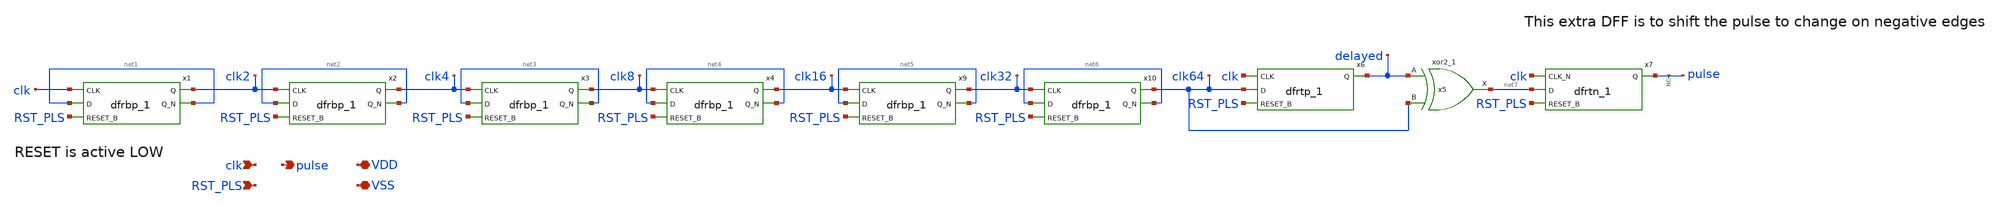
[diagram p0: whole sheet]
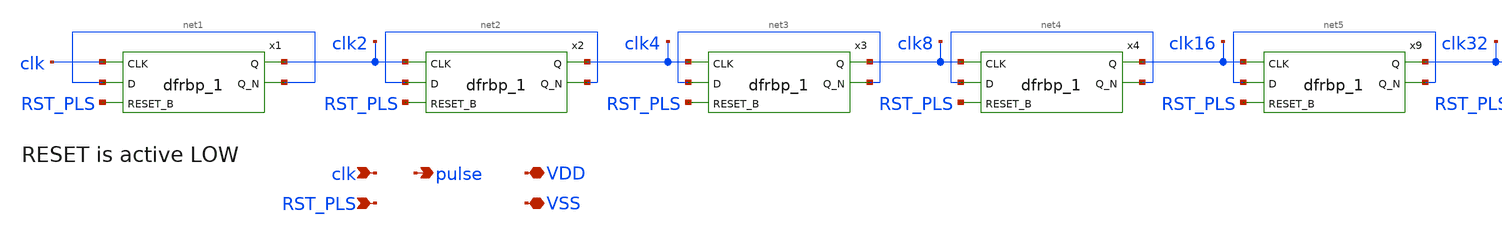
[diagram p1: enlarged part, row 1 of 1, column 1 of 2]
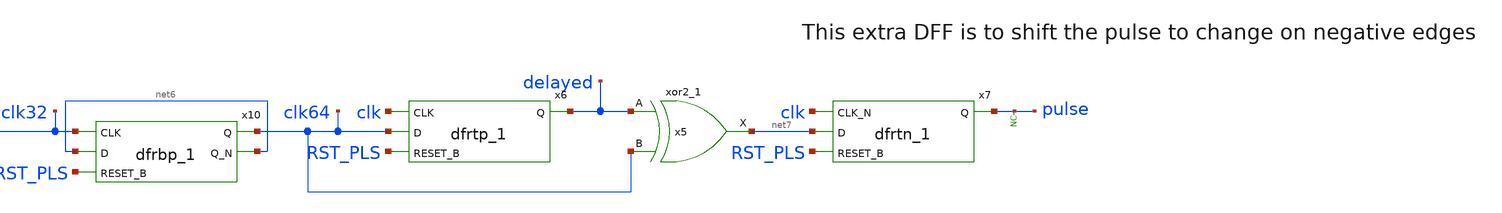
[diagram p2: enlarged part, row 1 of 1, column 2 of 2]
** sch_path: xschem/src/pulse_generator/pulse_generator.sch
**.subckt pulse_generator clk RST_PLS pulse VDD VSS
*.ipin clk
*.ipin RST_PLS
*.opin pulse
*.iopin VDD
*.iopin VSS
x1 clk net1 RST_PLS VSS VSS VDD VDD clk2 net1 sky130_fd_sc_hd__dfrbp_1
x2 clk2 net2 RST_PLS VSS VSS VDD VDD clk4 net2 sky130_fd_sc_hd__dfrbp_1
x3 clk4 net3 RST_PLS VSS VSS VDD VDD clk8 net3 sky130_fd_sc_hd__dfrbp_1
x4 clk8 net4 RST_PLS VSS VSS VDD VDD clk16 net4 sky130_fd_sc_hd__dfrbp_1
x5 delayed clk64 VSS VSS VDD VDD net7 sky130_fd_sc_hd__xor2_1
x9 clk16 net5 RST_PLS VSS VSS VDD VDD clk32 net5 sky130_fd_sc_hd__dfrbp_1
x10 clk32 net6 RST_PLS VSS VSS VDD VDD clk64 net6 sky130_fd_sc_hd__dfrbp_1
* noconn pulse
x6 clk clk64 RST_PLS VSS VSS VDD VDD delayed sky130_fd_sc_hd__dfrtp_1
x7 clk net7 RST_PLS VSS VSS VDD VDD pulse sky130_fd_sc_hd__dfrtn_1
**.ends
.end
